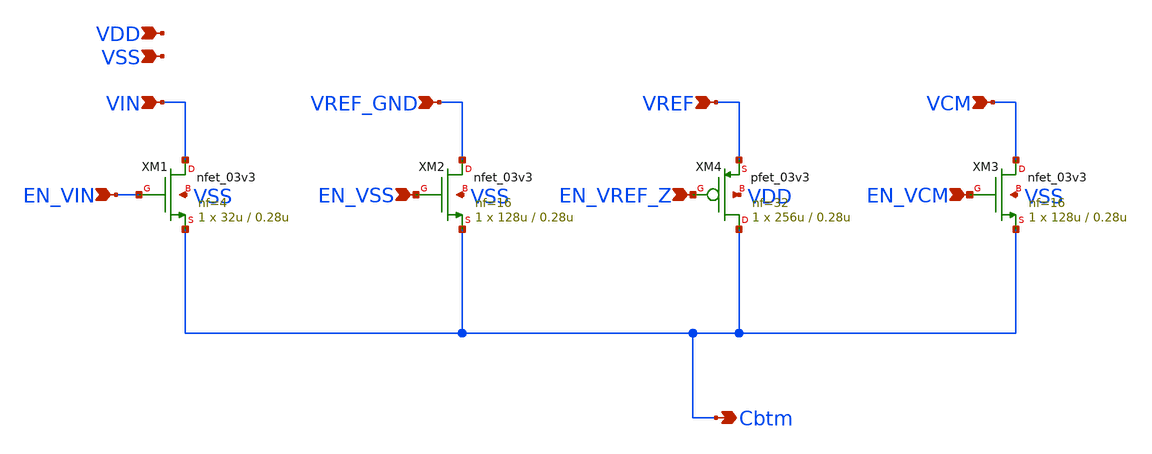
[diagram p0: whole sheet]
** sch_path: Schematic/individual_switch/switch_C10.sch
**.subckt switch_C10 VIN EN_VIN VREF_GND VREF VCM EN_VCM Cbtm VDD EN_VSS EN_VREF_Z VSS
*.ipin VIN
*.ipin EN_VIN
*.ipin VREF_GND
*.ipin VREF
*.ipin VCM
*.ipin EN_VCM
*.opin Cbtm
*.ipin VDD
*.ipin EN_VSS
*.ipin EN_VREF_Z
*.ipin VSS
XM1 VIN EN_VIN Cbtm VSS nfet_03v3 L=0.28u W=32u nf=4 ad='int((nf+1)/2) * W/nf * 0.18u' as='int((nf+2)/2) * W/nf * 0.18u'
+ pd='2*int((nf+1)/2) * (W/nf + 0.18u)' ps='2*int((nf+2)/2) * (W/nf + 0.18u)' nrd='0.18u / W' nrs='0.18u / W'
+ sa=0 sb=0 sd=0 m=1
XM2 VREF_GND EN_VSS Cbtm VSS nfet_03v3 L=0.28u W=128u nf=16 ad='int((nf+1)/2) * W/nf * 0.18u' as='int((nf+2)/2) * W/nf * 0.18u'
+ pd='2*int((nf+1)/2) * (W/nf + 0.18u)' ps='2*int((nf+2)/2) * (W/nf + 0.18u)' nrd='0.18u / W' nrs='0.18u / W'
+ sa=0 sb=0 sd=0 m=1
XM3 VCM EN_VCM Cbtm VSS nfet_03v3 L=0.28u W=128u nf=16 ad='int((nf+1)/2) * W/nf * 0.18u' as='int((nf+2)/2) * W/nf * 0.18u'
+ pd='2*int((nf+1)/2) * (W/nf + 0.18u)' ps='2*int((nf+2)/2) * (W/nf + 0.18u)' nrd='0.18u / W' nrs='0.18u / W'
+ sa=0 sb=0 sd=0 m=1
XM4 Cbtm EN_VREF_Z VREF VDD pfet_03v3 L=0.28u W=256u nf=32 ad='int((nf+1)/2) * W/nf * 0.18u' as='int((nf+2)/2) * W/nf * 0.18u'
+ pd='2*int((nf+1)/2) * (W/nf + 0.18u)' ps='2*int((nf+2)/2) * (W/nf + 0.18u)' nrd='0.18u / W' nrs='0.18u / W'
+ sa=0 sb=0 sd=0 m=1
**.ends
.end
